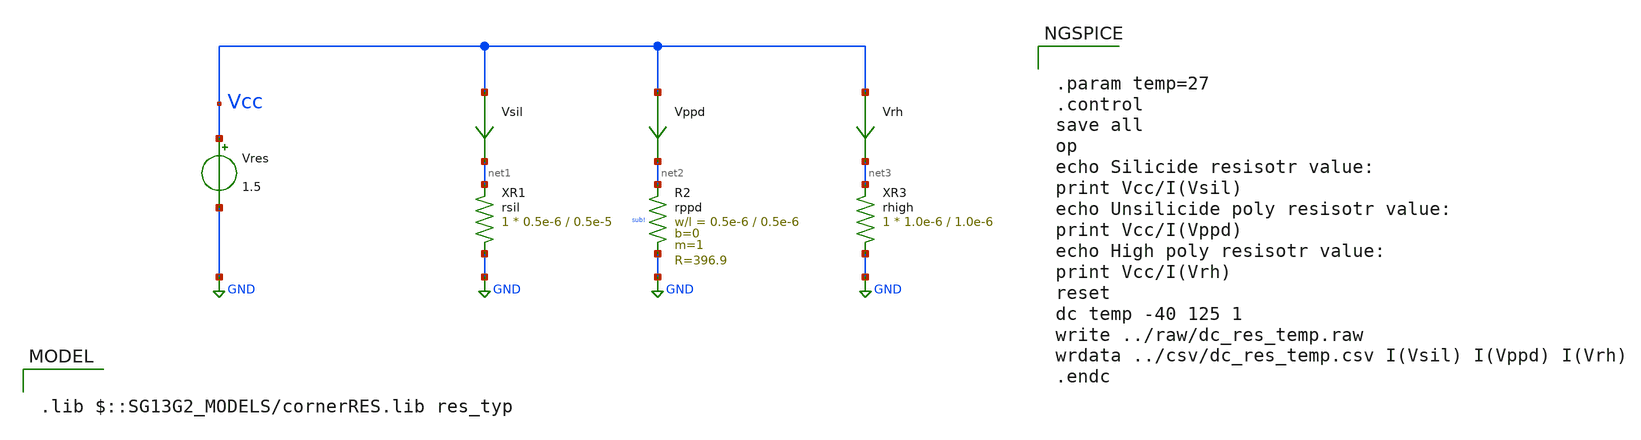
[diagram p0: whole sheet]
** sch_path: ihp-sg13g2/libs.tech/xschem/sg13g2_tests/dc_res_temp.sch
* Copyright 2023 IHP PDK Authors
**.subckt dc_res_temp
Vres Vcc GND 1.5
Vsil Vcc net1 0
.save i(vsil)
Vppd Vcc net2 0
.save i(vppd)
XR3 GND net3 rhigh w=1.0e-6 l=1.0e-6 m=1 R=3.061e+3 Imax=0.11e-4
Vrh Vcc net3 0
.save i(vrh)
XR1 GND net1 rsil w=0.5e-6 l=0.5e-5 m=1 R=7.0 Imax=0.3e-6
XR2 net2 GND sub! rppd w=0.5e-6 l=0.5e-6 m=1 b=0 mm_ok=1
**** begin user architecture code

.lib $::SG13G2_MODELS/cornerRES.lib res_typ



.param temp=27
.control
save all
op
echo Silicide resisotr value:
print Vcc/I(Vsil)
echo Unsilicide poly resisotr value:
print Vcc/I(Vppd)
echo High poly resisotr value:
print Vcc/I(Vrh)
reset
dc temp -40 125 1
write ../raw/dc_res_temp.raw
wrdata ../csv/dc_res_temp.csv I(Vsil) I(Vppd) I(Vrh)
.endc


**** end user architecture code
**.ends
.GLOBAL GND
.end
